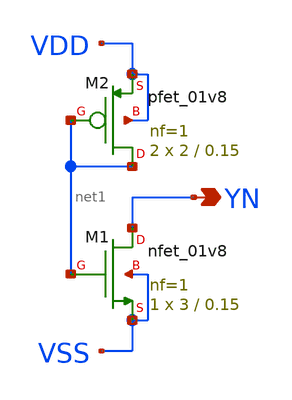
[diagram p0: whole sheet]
** sch_path: layout/xschem/sky130_rhbd/TIELO.sch
**.subckt TIELO YN
*.opin YN
XM1 YN net1 VSS VSS sky130_fd_pr__nfet_01v8 L=0.15 W=3 nf=1 ad='int((nf+1)/2) * W/nf * 0.29' as='int((nf+2)/2) * W/nf * 0.29'
+ pd='2*int((nf+1)/2) * (W/nf + 0.29)' ps='2*int((nf+2)/2) * (W/nf + 0.29)' nrd='0.29 / W' nrs='0.29 / W'
+ sa=0 sb=0 sd=0 mult=1 m=1
XM2 net1 net1 VDD VDD sky130_fd_pr__pfet_01v8 L=0.15 W=2 nf=1 ad='int((nf+1)/2) * W/nf * 0.29' as='int((nf+2)/2) * W/nf * 0.29'
+ pd='2*int((nf+1)/2) * (W/nf + 0.29)' ps='2*int((nf+2)/2) * (W/nf + 0.29)' nrd='0.29 / W' nrs='0.29 / W'
+ sa=0 sb=0 sd=0 mult=2 m=2
**.ends
.end
